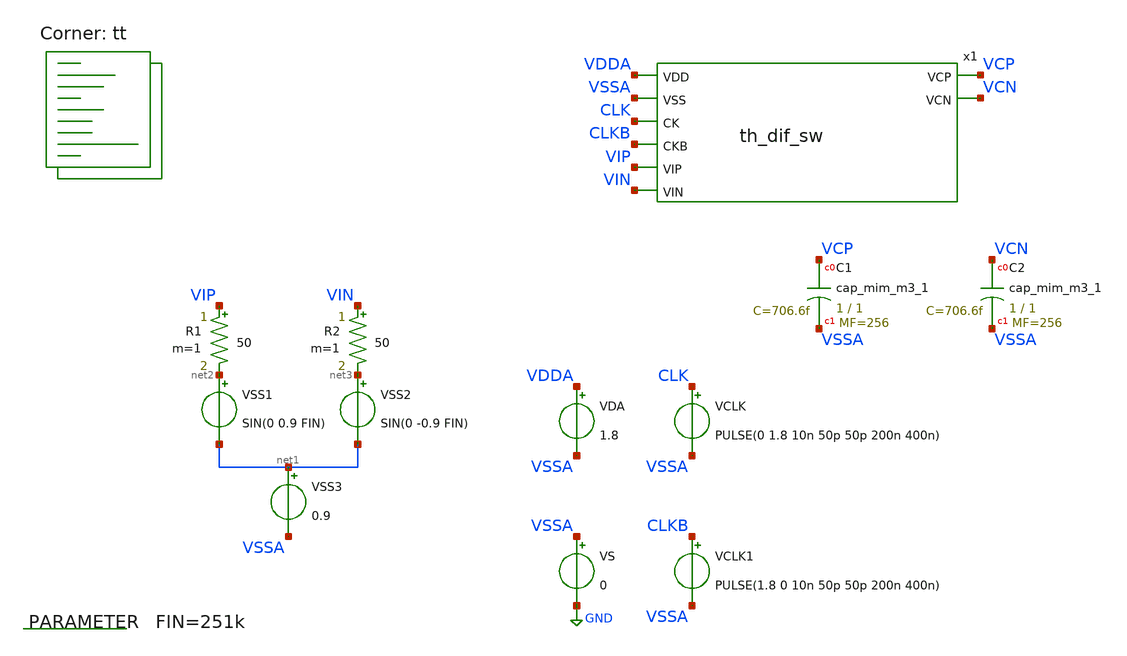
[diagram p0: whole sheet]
** sch_path: xschem/th_sw_tb.sch
**.subckt th_sw_tb
VS VSSA GND 0
VDA VDDA VSSA 1.8
VSS1 net2 net1 SIN(0 0.9 FIN)
VSS2 net3 net1 SIN(0 -0.9 FIN)
VSS3 net1 VSSA 0.9
VCLK CLK VSSA PULSE(0 1.8 10n 50p 50p 200n 400n)
R1 VIP net2 50 m=1
R2 VIN net3 50 m=1
x1 VDDA VSSA CLK CLKB VIP VIN VCP VCN th_dif_sw
VCLK1 CLKB VSSA PULSE(1.8 0 10n 50p 50p 200n 400n)
XC1 VCP VSSA sky130_fd_pr__cap_mim_m3_1 W=1 L=1 MF=256 m=256
XC2 VCN VSSA sky130_fd_pr__cap_mim_m3_1 W=1 L=1 MF=256 m=256
.param FIN=251k
**** begin user architecture code

** opencircuitdesign pdks install
* .lib $::SKYWATER_MODELS/sky130.lib.spice tt
.include $PDK_ROOT/$PDK/libs.ref/sky130_fd_sc_hd/spice/sky130_fd_sc_hd.spice



.option wnflag=0
.option savecurrents
.options method=trapezoid
.options solver=iterative
.control
global netlist_dir .
set wr_singlescale
save all
tran 100p 102.4u  ; Mengubah start time menjadi 1n
remzerovec
write th_sw_tb.raw
exit 1
.endc

.lib $::SKYWATER_MODELS/sky130.lib.spice tt
**** end user architecture code
**.ends

* expanding   symbol:  th_dif_sw.sym # of pins=8
** sym_path: xschem/th_dif_sw.sym
** sch_path: xschem/th_dif_sw.sch
.subckt th_dif_sw VDD VSS CK CKB VIP VIN VCP VCN
*.ipin VDD
*.ipin VSS
*.ipin CK
*.ipin CKB
*.ipin VIP
*.ipin VIN
*.opin VCP
*.opin VCN
x1 VDD VSS CK_BUFF CKB_BUFF VIP VCP th_sw
x2 VDD VSS CK_BUFF CKB_BUFF VIN VCN th_sw
x3 CK VSS VSS VDD VDD CK_BUFF sky130_fd_sc_hs__buf_16
x4 CKB VSS VSS VDD VDD CKB_BUFF sky130_fd_sc_hs__buf_16
**** begin user architecture code

.include /usr/local/share/pdk/sky130A/libs.ref/sky130_fd_sc_hs/spice/sky130_fd_sc_hs.spice

**** end user architecture code
.ends


* expanding   symbol:  th_sw.sym # of pins=6
** sym_path: xschem/th_sw.sym
** sch_path: xschem/th_sw.sch
.subckt th_sw VDD VSS CK CKB IN OUT
*.ipin VDD
*.ipin VSS
*.ipin CK
*.ipin CKB
*.ipin IN
*.opin OUT
XM1 net1 CKB VDD VDD sky130_fd_pr__pfet_01v8 L=0.15 W=3 nf=1 ad='int((nf+1)/2) * W/nf * 0.29' as='int((nf+2)/2) * W/nf * 0.29'
+ pd='2*int((nf+1)/2) * (W/nf + 0.29)' ps='2*int((nf+2)/2) * (W/nf + 0.29)' nrd='0.29 / W' nrs='0.29 / W'
+ sa=0 sb=0 sd=0 mult=1 m=1
XM2 net2 VGS VDD net2 sky130_fd_pr__pfet_01v8 L=0.15 W=1 nf=1 ad='int((nf+1)/2) * W/nf * 0.29' as='int((nf+2)/2) * W/nf * 0.29'
+ pd='2*int((nf+1)/2) * (W/nf + 0.29)' ps='2*int((nf+2)/2) * (W/nf + 0.29)' nrd='0.29 / W' nrs='0.29 / W'
+ sa=0 sb=0 sd=0 mult=1 m=1
XM3 VGS net1 net2 net2 sky130_fd_pr__pfet_01v8 L=0.15 W=1 nf=1 ad='int((nf+1)/2) * W/nf * 0.29' as='int((nf+2)/2) * W/nf * 0.29'
+ pd='2*int((nf+1)/2) * (W/nf + 0.29)' ps='2*int((nf+2)/2) * (W/nf + 0.29)' nrd='0.29 / W' nrs='0.29 / W'
+ sa=0 sb=0 sd=0 mult=1 m=1
XM4 net1 CKB net4 VSS sky130_fd_pr__nfet_01v8 L=0.15 W=1 nf=1 ad='int((nf+1)/2) * W/nf * 0.29' as='int((nf+2)/2) * W/nf * 0.29'
+ pd='2*int((nf+1)/2) * (W/nf + 0.29)' ps='2*int((nf+2)/2) * (W/nf + 0.29)' nrd='0.29 / W' nrs='0.29 / W'
+ sa=0 sb=0 sd=0 mult=1 m=1
XM5 net4 CK VSS VSS sky130_fd_pr__nfet_01v8 L=0.15 W=1 nf=1 ad='int((nf+1)/2) * W/nf * 0.29' as='int((nf+2)/2) * W/nf * 0.29'
+ pd='2*int((nf+1)/2) * (W/nf + 0.29)' ps='2*int((nf+2)/2) * (W/nf + 0.29)' nrd='0.29 / W' nrs='0.29 / W'
+ sa=0 sb=0 sd=0 mult=1 m=1
XM6 net1 VGS net4 VSS sky130_fd_pr__nfet_01v8 L=0.15 W=1 nf=1 ad='int((nf+1)/2) * W/nf * 0.29' as='int((nf+2)/2) * W/nf * 0.29'
+ pd='2*int((nf+1)/2) * (W/nf + 0.29)' ps='2*int((nf+2)/2) * (W/nf + 0.29)' nrd='0.29 / W' nrs='0.29 / W'
+ sa=0 sb=0 sd=0 mult=1 m=1
XM7 IN VGS net4 VSS sky130_fd_pr__nfet_01v8 L=0.15 W=1 nf=1 ad='int((nf+1)/2) * W/nf * 0.29' as='int((nf+2)/2) * W/nf * 0.29'
+ pd='2*int((nf+1)/2) * (W/nf + 0.29)' ps='2*int((nf+2)/2) * (W/nf + 0.29)' nrd='0.29 / W' nrs='0.29 / W'
+ sa=0 sb=0 sd=0 mult=1 m=1
XM8 VGS VDD net3 VSS sky130_fd_pr__nfet_01v8 L=0.15 W=1 nf=1 ad='int((nf+1)/2) * W/nf * 0.29' as='int((nf+2)/2) * W/nf * 0.29'
+ pd='2*int((nf+1)/2) * (W/nf + 0.29)' ps='2*int((nf+2)/2) * (W/nf + 0.29)' nrd='0.29 / W' nrs='0.29 / W'
+ sa=0 sb=0 sd=0 mult=1 m=1
XM9 net3 CK VSS VSS sky130_fd_pr__nfet_01v8 L=0.15 W=1 nf=1 ad='int((nf+1)/2) * W/nf * 0.29' as='int((nf+2)/2) * W/nf * 0.29'
+ pd='2*int((nf+1)/2) * (W/nf + 0.29)' ps='2*int((nf+2)/2) * (W/nf + 0.29)' nrd='0.29 / W' nrs='0.29 / W'
+ sa=0 sb=0 sd=0 mult=1 m=1
XC1 net2 net4 sky130_fd_pr__cap_mim_m3_1 W=4 L=4 MF=8 m=8
XM10 OUT VGS IN VSS sky130_fd_pr__nfet_01v8 L=0.15 W=8 nf=1 ad='int((nf+1)/2) * W/nf * 0.29' as='int((nf+2)/2) * W/nf * 0.29'
+ pd='2*int((nf+1)/2) * (W/nf + 0.29)' ps='2*int((nf+2)/2) * (W/nf + 0.29)' nrd='0.29 / W' nrs='0.29 / W'
+ sa=0 sb=0 sd=0 mult=1 m=1
XM11 IN CK IN VSS sky130_fd_pr__nfet_01v8 L=0.15 W=8 nf=1 ad='int((nf+1)/2) * W/nf * 0.29' as='int((nf+2)/2) * W/nf * 0.29'
+ pd='2*int((nf+1)/2) * (W/nf + 0.29)' ps='2*int((nf+2)/2) * (W/nf + 0.29)' nrd='0.29 / W' nrs='0.29 / W'
+ sa=0 sb=0 sd=0 mult=1 m=1
XM12 OUT CK OUT VSS sky130_fd_pr__nfet_01v8 L=0.15 W=8 nf=1 ad='int((nf+1)/2) * W/nf * 0.29' as='int((nf+2)/2) * W/nf * 0.29'
+ pd='2*int((nf+1)/2) * (W/nf + 0.29)' ps='2*int((nf+2)/2) * (W/nf + 0.29)' nrd='0.29 / W' nrs='0.29 / W'
+ sa=0 sb=0 sd=0 mult=1 m=1
.ends

.GLOBAL GND
.end
